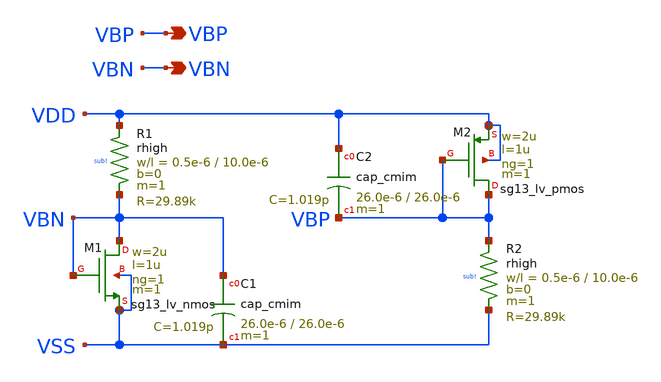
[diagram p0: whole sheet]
** sch_path: design/blocks/bias/schematic/bias.sch
**.subckt bias VBP VBN
*.opin VBP
*.opin VBN
XM1 VBN VBN VSS VSS sg13_lv_nmos w=2u l=1u ng=1 m=1 mm_ok=1
XM2 VBP VBP VDD VDD sg13_lv_pmos w=2u l=1u ng=1 m=1 mm_ok=1
XR2 VBP VSS sub! rhigh w=0.5e-6 l=10.0e-6 m=1 b=0 mm_ok=1
XR1 VDD VBN sub! rhigh w=0.5e-6 l=10.0e-6 m=1 b=0 mm_ok=1
XC1 VBN VSS cap_cmim w=26.0e-6 l=26.0e-6 m=1 mm_ok=1
XC2 VDD VBP cap_cmim w=26.0e-6 l=26.0e-6 m=1 mm_ok=1
**.ends
.end
